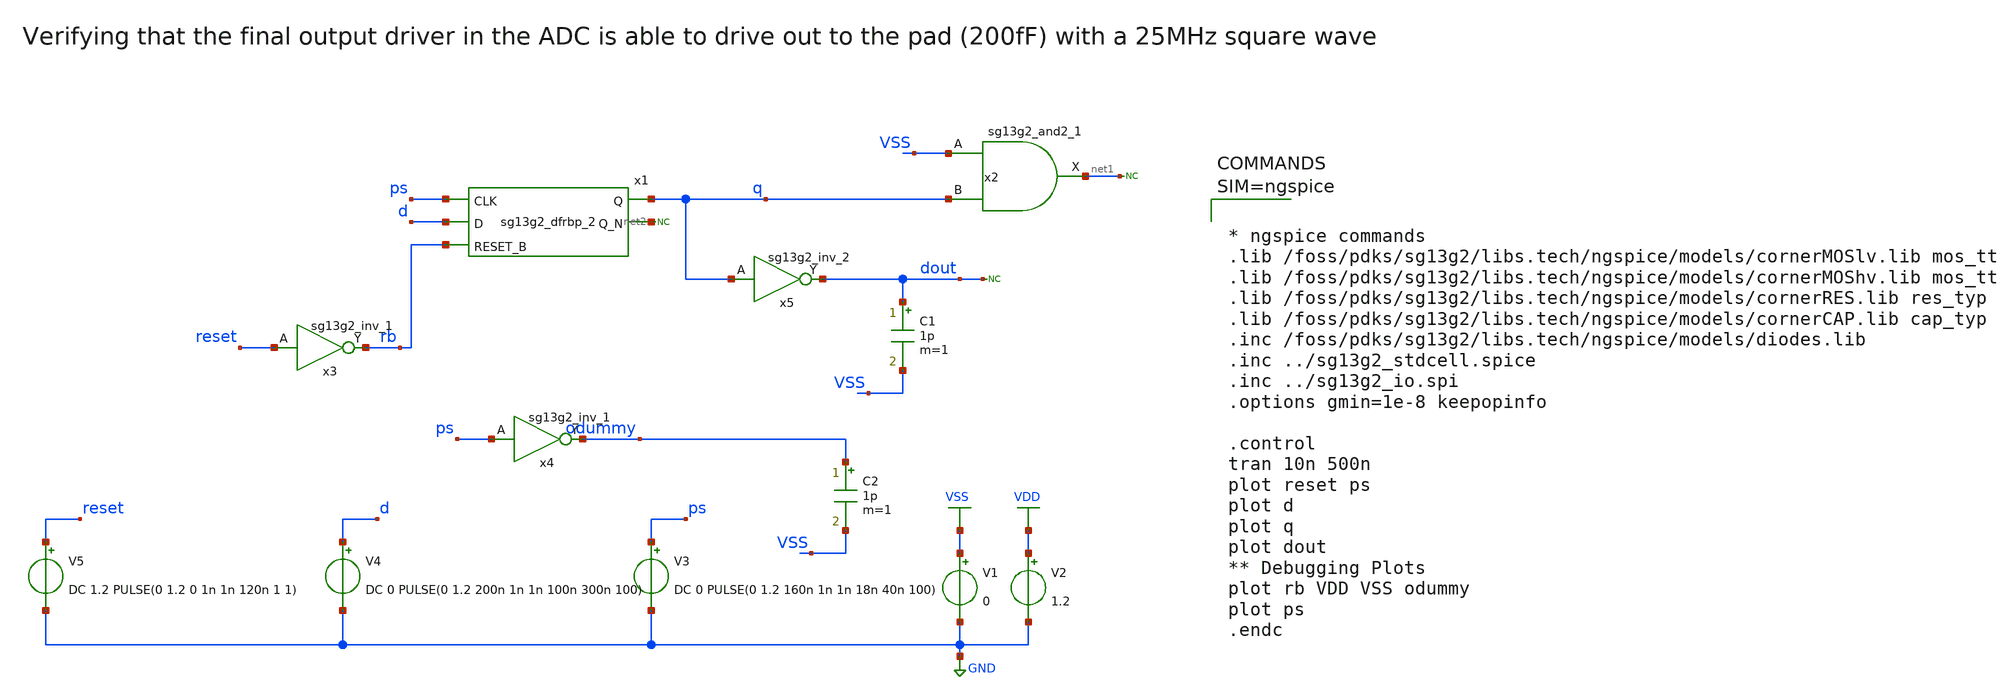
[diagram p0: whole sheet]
** sch_path: 5_Design/3_Real_circuits/tb_digital_driver_strength.sch
* IHP-GmbH/IHP-Open-PDK/ihp-sg13g2/libs.tech/xschem/sg13g2_stdcells/sg13g2_inv_2.sch:
* Copyright 2023 IHP PDK Authors
* Licensed under the Apache License, Version 2.0 (the "License");
**.subckt tb_digital_driver_strength
x1 q net2 ps d rb VDD VSS sg13g2_dfrbp_2
x3 rb reset VDD VSS sg13g2_inv_1
x5 dout q VDD VSS sg13g2_inv_2
* noconn #net2
x2 net1 VSS q VDD VSS sg13g2_and2_1
V2 VDD GND 1.2
V3 ps GND DC 0 PULSE(0 1.2 160n 1n 1n 18n 40n 100)
* noconn #net1
C1 dout VSS 1p m=1
V4 d GND DC 0 PULSE(0 1.2 200n 1n 1n 100n 300n 100)
V5 reset GND DC 1.2 PULSE(0 1.2 0 1n 1n 120n 1 1)
x4 odummy ps VDD VSS sg13g2_inv_1
V1 VSS GND 0
* noconn dout
C2 odummy VSS 1p m=1
**** begin user architecture code



* ngspice commands
.lib /foss/pdks/sg13g2/libs.tech/ngspice/models/cornerMOSlv.lib mos_tt
.lib /foss/pdks/sg13g2/libs.tech/ngspice/models/cornerMOShv.lib mos_tt
.lib /foss/pdks/sg13g2/libs.tech/ngspice/models/cornerRES.lib res_typ
.lib /foss/pdks/sg13g2/libs.tech/ngspice/models/cornerCAP.lib cap_typ
.inc /foss/pdks/sg13g2/libs.tech/ngspice/models/diodes.lib
.inc ../sg13g2_stdcell.spice
.inc ../sg13g2_io.spi
.options gmin=1e-8 keepopinfo

.control
tran 10n 500n
plot reset ps
plot d
plot q
plot dout
** Debugging Plots
plot rb VDD VSS odummy
plot ps
.endc


**** end user architecture code
**.ends

* expanding   symbol:  sg13g2_stdcells/sg13g2_dfrbp_2.sym # of pins=5
** sym_path: sg13g2_stdcells/sg13g2_dfrbp_2.sym
** sch_path: sg13g2_stdcells/sg13g2_dfrbp_2.sch
.subckt sg13g2_dfrbp_2 Q Q_N CLK D RESET_B VDD VSS
*.ipin D
*.ipin RESET_B
*.ipin CLK
*.opin Q
*.opin Q_N
*.iopin VDD
*.iopin VSS
XM1 Db D net12 VSS sg13_lv_nmos w=420.00n l=130.00n ng=1 m=1 mm_ok=1
XM2 net12 RESET_B VSS VSS sg13_lv_nmos w=420.00n l=130.00n ng=1 m=1 mm_ok=1
XM3 net2 clkneg net11 VSS sg13_lv_nmos w=420.00n l=130.00n ng=1 m=1 mm_ok=1
XM4 net11 net3 VSS VSS sg13_lv_nmos w=420.00n l=130.00n ng=1 m=1 mm_ok=1
XM5 net3 net2 net7 VSS sg13_lv_nmos w=420.00n l=130.00n ng=1 m=1 mm_ok=1
XM6 net7 RESET_B VSS VSS sg13_lv_nmos w=420.00n l=130.00n ng=1 m=1 mm_ok=1
XM7 Q_N net2 VSS VSS sg13_lv_nmos w=1.48u l=130.00n ng=2 m=1 mm_ok=1
XM8 net1 net2 VSS VSS sg13_lv_nmos w=640.00n l=130.00n ng=1 m=1 mm_ok=1
XM9 Q net1 VSS VSS sg13_lv_nmos w=1.48u l=130.00n ng=2 m=1 mm_ok=1
XM10 clkneg CLK VSS VSS sg13_lv_nmos w=740.00n l=130.00n ng=1 m=1 mm_ok=1
XM11 clkpos clkneg VSS VSS sg13_lv_nmos w=740.00n l=130.00n ng=1 m=1 mm_ok=1
XM12 Db clkneg net4 VSS sg13_lv_nmos w=420.00n l=130.00n ng=1 m=1 mm_ok=1
XM13 net4 clkpos net10 VSS sg13_lv_nmos w=420.00n l=130.00n ng=1 m=1 mm_ok=1
XM14 net10 net5 net6 VSS sg13_lv_nmos w=420.00n l=130.00n ng=1 m=1 mm_ok=1
XM15 net6 RESET_B VSS VSS sg13_lv_nmos w=420.00n l=130.00n ng=1 m=1 mm_ok=1
XM16 net5 net4 VSS VSS sg13_lv_nmos w=740.00n l=130.00n ng=1 m=1 mm_ok=1
XM17 net5 clkpos net2 VSS sg13_lv_nmos w=740.00n l=130.00n ng=1 m=1 mm_ok=1
XM18 Db RESET_B VDD VDD sg13_lv_pmos w=420.00n l=130.00n ng=1 m=1 mm_ok=1
XM19 Db D VDD VDD sg13_lv_pmos w=420.00n l=130.00n ng=1 m=1 mm_ok=1
XM20 net9 net3 VDD VDD sg13_lv_pmos w=420.00n l=130.00n ng=1 m=1 mm_ok=1
XM21 net2 clkpos net9 VDD sg13_lv_pmos w=420.00n l=130.00n ng=1 m=1 mm_ok=1
XM22 net3 net2 VDD VDD sg13_lv_pmos w=420.00n l=130.00n ng=1 m=1 mm_ok=1
XM23 net3 RESET_B VDD VDD sg13_lv_pmos w=420.00n l=130.00n ng=1 m=1 mm_ok=1
XM24 Q_N net2 VDD VDD sg13_lv_pmos w=2.24u l=130.00n ng=2 m=1 mm_ok=1
XM25 net1 net2 VDD VDD sg13_lv_pmos w=1.000u l=130.00n ng=1 m=1 mm_ok=1
XM26 Q net1 VDD VDD sg13_lv_pmos w=2.24u l=130.00n ng=2 m=1 mm_ok=1
XM27 clkneg CLK VDD VDD sg13_lv_pmos w=1.12u l=130.00n ng=1 m=1 mm_ok=1
XM28 clkpos clkneg VDD VDD sg13_lv_pmos w=1.12u l=130.00n ng=1 m=1 mm_ok=1
XM29 Db clkpos net4 VDD sg13_lv_pmos w=420.00n l=130.00n ng=1 m=1 mm_ok=1
XM30 net8 net5 VDD VDD sg13_lv_pmos w=420.00n l=130.00n ng=1 m=1 mm_ok=1
XM31 net4 clkneg net8 VDD sg13_lv_pmos w=420.00n l=130.00n ng=1 m=1 mm_ok=1
XM32 net4 RESET_B VDD VDD sg13_lv_pmos w=420.00n l=130.00n ng=1 m=1 mm_ok=1
XM33 net5 net4 VDD VDD sg13_lv_pmos w=1.000u l=130.00n ng=1 m=1 mm_ok=1
XM34 net5 clkneg net2 VDD sg13_lv_pmos w=1.000u l=130.00n ng=1 m=1 mm_ok=1
.ends


* expanding   symbol:  sg13g2_stdcells/sg13g2_inv_1.sym # of pins=2
** sym_path: sg13g2_stdcells/sg13g2_inv_1.sym
** sch_path: sg13g2_stdcells/sg13g2_inv_1.sch
.subckt sg13g2_inv_1 Y A VDD VSS
*.opin Y
*.ipin A
*.iopin VDD
*.iopin VSS
XM1 Y A VSS VSS sg13_lv_nmos w=740.00n l=130.00n ng=1 m=1 mm_ok=1
XM2 Y A VDD VDD sg13_lv_pmos w=1.12u l=130.00n ng=1 m=1 mm_ok=1
.ends


* expanding   symbol:  sg13g2_stdcells/sg13g2_inv_2.sym # of pins=2
** sym_path: sg13g2_stdcells/sg13g2_inv_2.sym
** sch_path: sg13g2_stdcells/sg13g2_inv_2.sch
.subckt sg13g2_inv_2 Y A VDD VSS
*.opin Y
*.ipin A
*.iopin VDD
*.iopin VSS
XM1 Y A VSS VSS sg13_lv_nmos w=1.48u l=130.00n ng=2 m=1 mm_ok=1
XM2 Y A VDD VDD sg13_lv_pmos w=2.24u l=130.00n ng=2 m=1 mm_ok=1
.ends


* expanding   symbol:  sg13g2_stdcells/sg13g2_and2_1.sym # of pins=3
** sym_path: sg13g2_stdcells/sg13g2_and2_1.sym
** sch_path: sg13g2_stdcells/sg13g2_and2_1.sch
.subckt sg13g2_and2_1 X A B VDD VSS
*.ipin A
*.ipin B
*.opin X
*.iopin VDD
*.iopin VSS
XM1 net1 A net2 VSS sg13_lv_nmos w=640.00n l=130.00n ng=1 m=1 mm_ok=1
XM2 net2 B VSS VSS sg13_lv_nmos w=640.00n l=130.00n ng=1 m=1 mm_ok=1
XM3 X net1 VSS VSS sg13_lv_nmos w=740.00n l=130.00n ng=1 m=1 mm_ok=1
XM4 net1 B VDD VDD sg13_lv_pmos w=840.00n l=130.00n ng=1 m=1 mm_ok=1
XM5 net1 A VDD VDD sg13_lv_pmos w=840.00n l=130.00n ng=1 m=1 mm_ok=1
XM6 X net1 VDD VDD sg13_lv_pmos w=1.12u l=130.00n ng=1 m=1 mm_ok=1
.ends

.GLOBAL VSS
.GLOBAL VDD
.GLOBAL GND
.end
